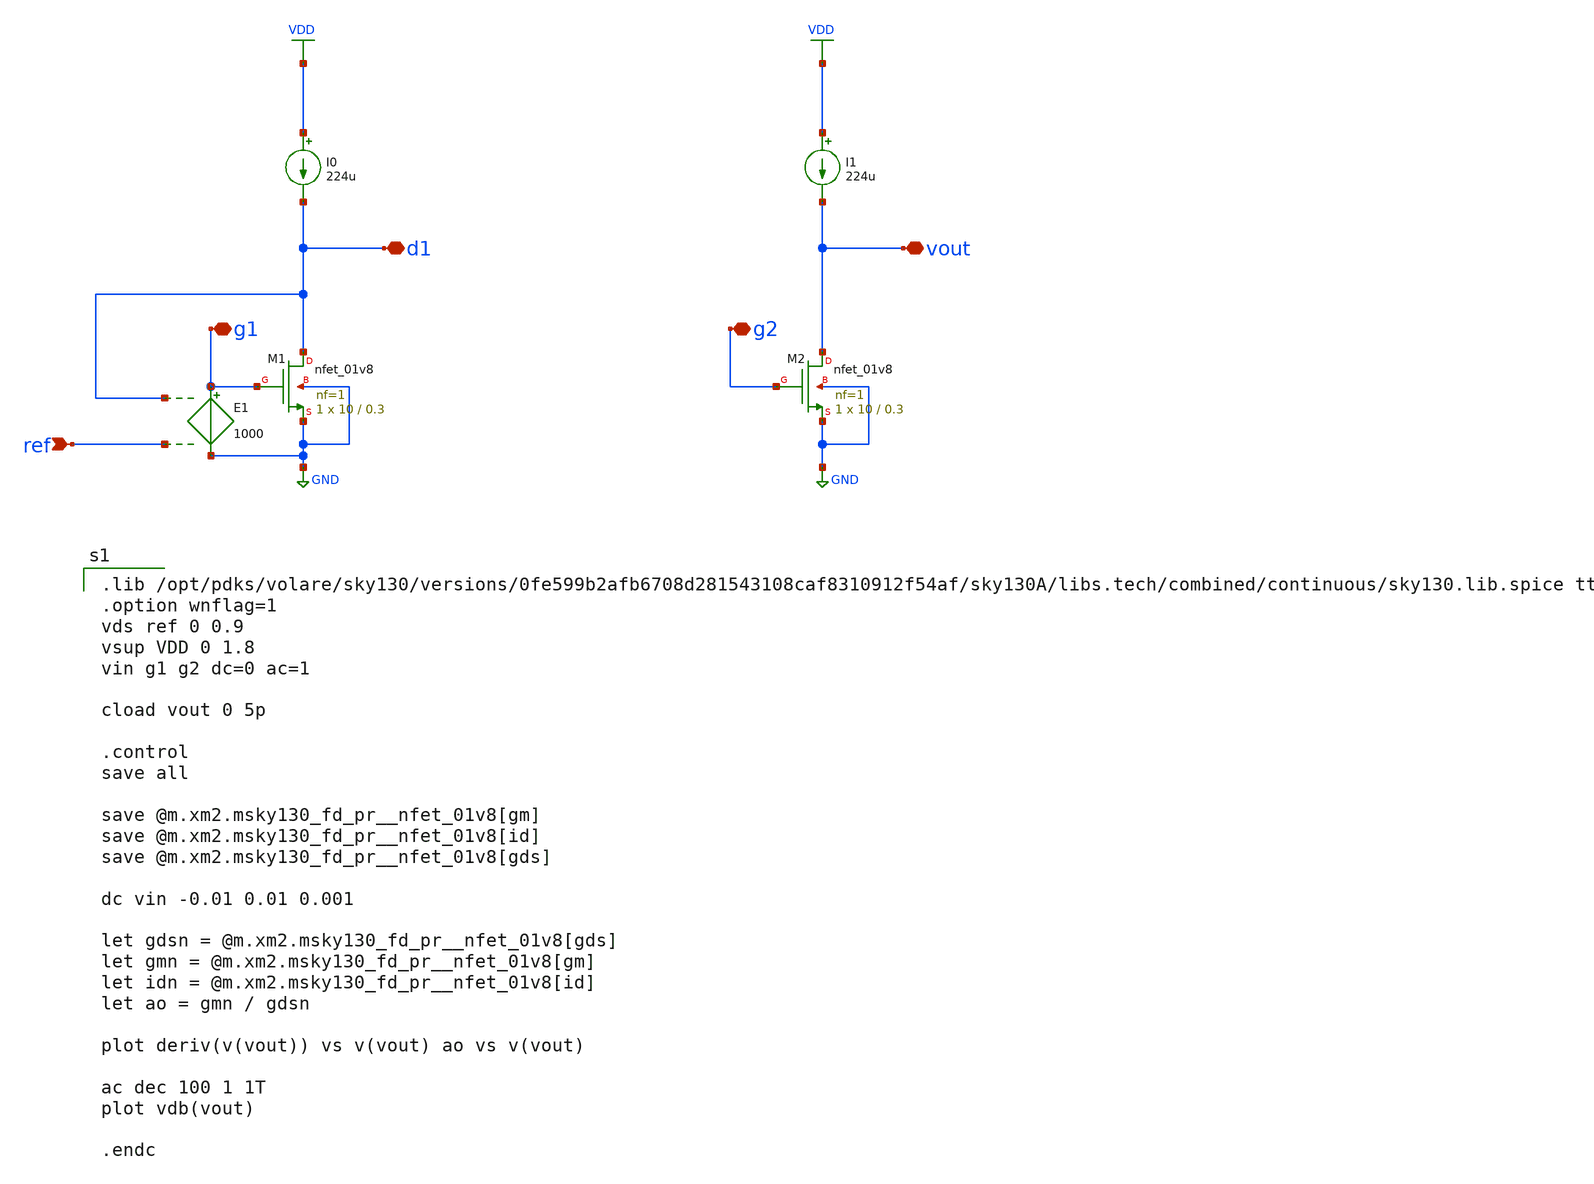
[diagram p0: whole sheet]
** sch_path: sky130_cs_amp_full.sch
**.subckt sky130_cs_amp_full ref g1 d1 g2 vout
*.ipin ref
*.iopin g1
*.iopin d1
*.iopin g2
*.iopin vout
E1 g1 GND d1 ref 1000
I0 VDD d1 224u
I1 VDD vout 224u
XM1 d1 g1 GND GND sky130_fd_pr__nfet_01v8 L=0.3 W=10 nf=1 ad='int((nf+1)/2) * W/nf * 0.29' as='int((nf+2)/2) * W/nf * 0.29'
+ pd='2*int((nf+1)/2) * (W/nf + 0.29)' ps='2*int((nf+2)/2) * (W/nf + 0.29)' nrd='0.29 / W' nrs='0.29 / W'
+ sa=0 sb=0 sd=0 mult=1 m=1
XM2 vout g2 GND GND sky130_fd_pr__nfet_01v8 L=0.3 W=10 nf=1 ad='int((nf+1)/2) * W/nf * 0.29' as='int((nf+2)/2) * W/nf * 0.29'
+ pd='2*int((nf+1)/2) * (W/nf + 0.29)' ps='2*int((nf+2)/2) * (W/nf + 0.29)' nrd='0.29 / W' nrs='0.29 / W'
+ sa=0 sb=0 sd=0 mult=1 m=1
**** begin user architecture code

.lib /opt/pdks/volare/sky130/versions/0fe599b2afb6708d281543108caf8310912f54af/sky130A/libs.tech/combined/continuous/sky130.lib.spice tt
.option wnflag=1
vds ref 0 0.9
vsup VDD 0 1.8
vin g1 g2 dc=0 ac=1

cload vout 0 5p

.control
save all

save @m.xm2.msky130_fd_pr__nfet_01v8[gm]
save @m.xm2.msky130_fd_pr__nfet_01v8[id]
save @m.xm2.msky130_fd_pr__nfet_01v8[gds]

dc vin -0.01 0.01 0.001

let gdsn = @m.xm2.msky130_fd_pr__nfet_01v8[gds]
let gmn = @m.xm2.msky130_fd_pr__nfet_01v8[gm]
let idn = @m.xm2.msky130_fd_pr__nfet_01v8[id]
let ao = gmn / gdsn

plot deriv(v(vout)) vs v(vout) ao vs v(vout)

ac dec 100 1 1T
plot vdb(vout)

.endc

**** end user architecture code
**.ends
.GLOBAL GND
.GLOBAL VDD
.end
